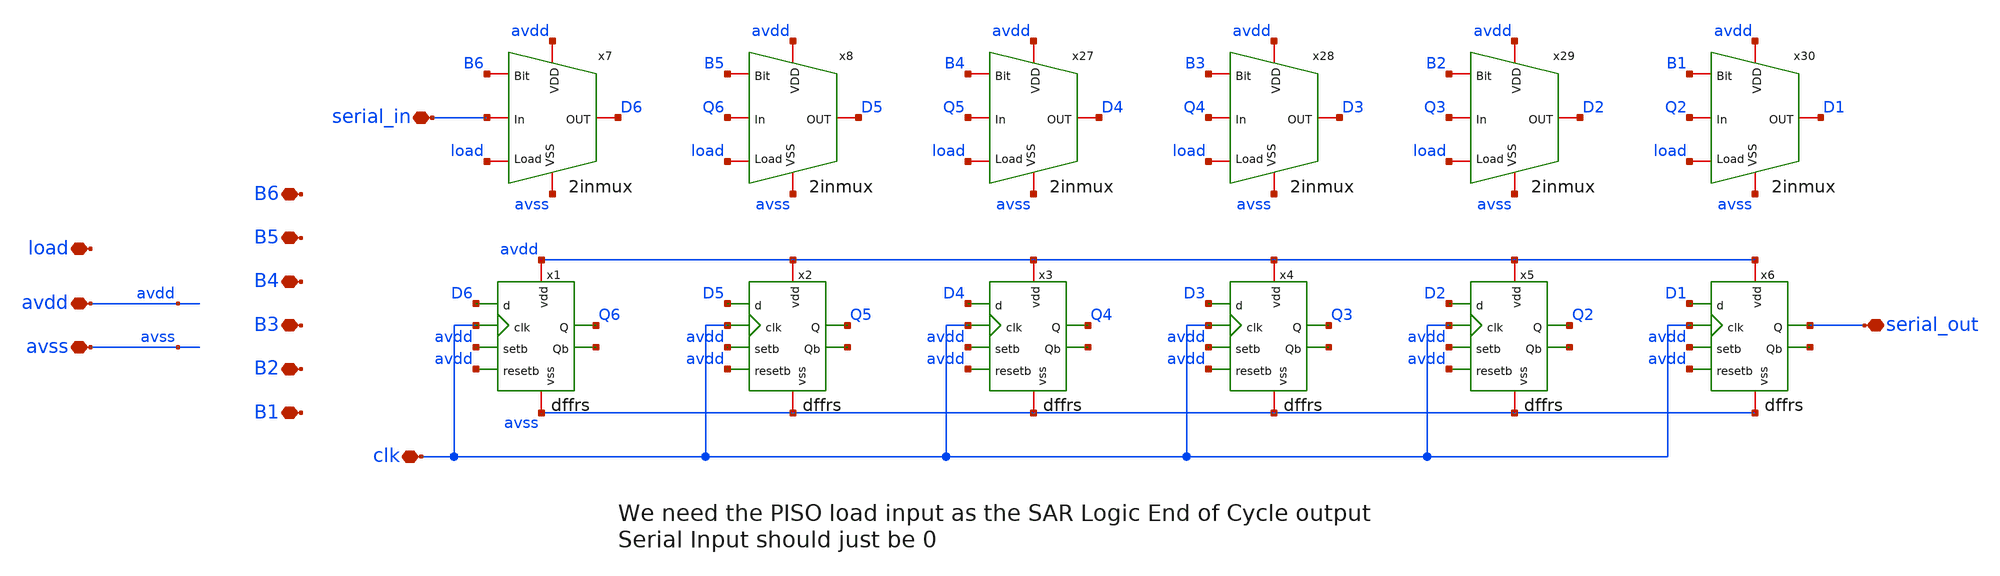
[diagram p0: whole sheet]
** sch_path: designs/FinalBlocksLayout/piso/adc_PISO.sch
**.subckt adc_PISO avdd avss clk B6 B5 B4 B3 B2 B1 load serial_out serial_in
*.iopin avdd
*.iopin avss
*.iopin clk
*.iopin B6
*.iopin B5
*.iopin B4
*.iopin B3
*.iopin B2
*.iopin B1
*.iopin load
*.iopin serial_out
*.iopin serial_in
x7 B6 load avdd D6 avss serial_in 2inmux
x8 B5 load avdd D5 avss Q6 2inmux
x27 B4 load avdd D4 avss Q5 2inmux
x28 B3 load avdd D3 avss Q4 2inmux
x29 B2 load avdd D2 avss Q3 2inmux
x30 B1 load avdd D1 avss Q2 2inmux
x1 avdd avss D6 clk avdd avdd Q6 net1 dffrs
x2 avdd avss D5 clk avdd avdd Q5 net2 dffrs
x3 avdd avss D4 clk avdd avdd Q4 net3 dffrs
x4 avdd avss D3 clk avdd avdd Q3 net4 dffrs
x5 avdd avss D2 clk avdd avdd Q2 net5 dffrs
x6 avdd avss D1 clk avdd avdd serial_out net6 dffrs
**.ends
.end
